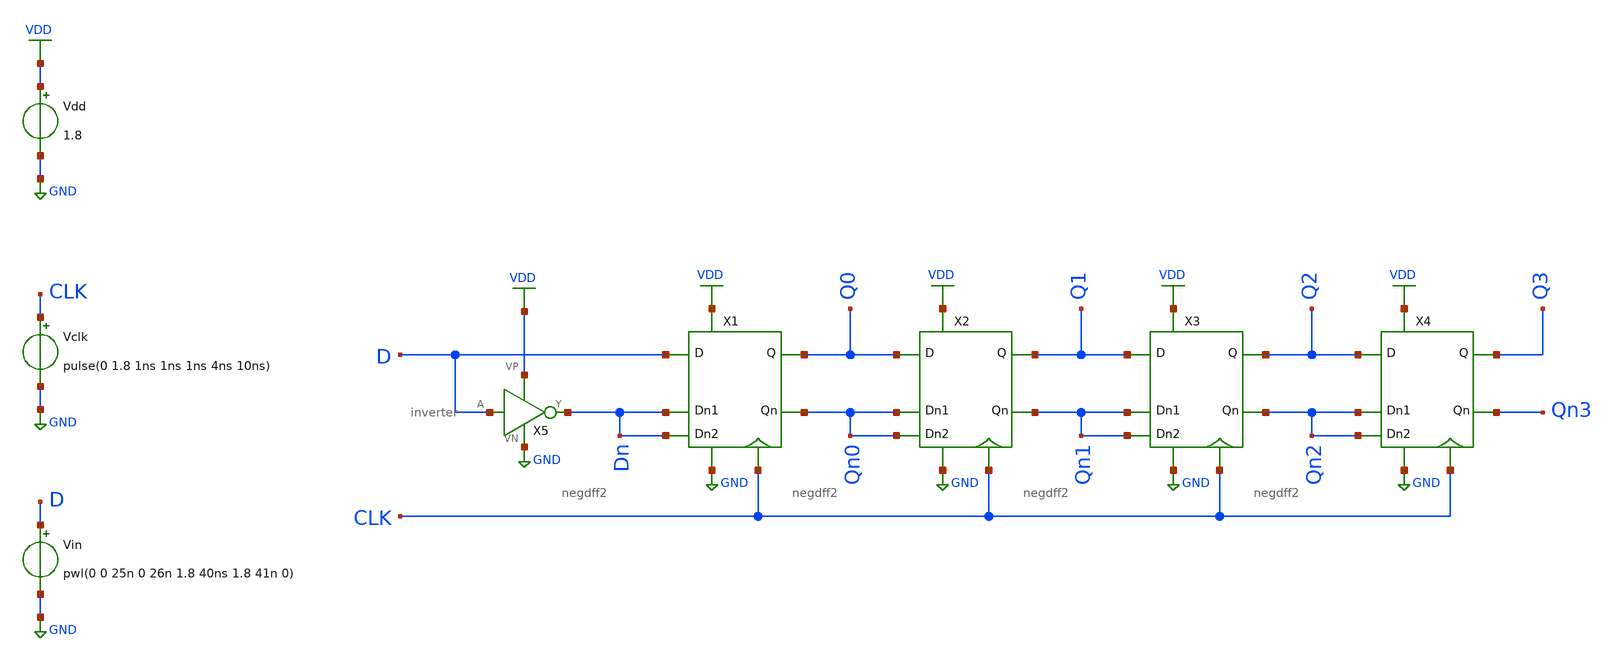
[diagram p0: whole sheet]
** sch_path: projects/negdff/xschem_ngspice/sreg_tran.sch
**.subckt sreg_tran
X1 VDD GND CLK D Dn Dn Q0 Qn0 negdff2
X2 VDD GND CLK Q0 Qn0 Qn0 Q1 Qn1 negdff2
X3 VDD GND CLK Q1 Qn1 Qn1 Q2 Qn2 negdff2
X4 VDD GND CLK Q2 Qn2 Qn2 Q3 Qn3 negdff2
X5 D Dn VDD GND inverter
Vin D GND pwl(0 0 25n 0 26n 1.8 40ns 1.8 41n 0)
Vdd VDD GND 1.8
Vclk CLK GND pulse(0 1.8 1ns 1ns 1ns 4ns 10ns)
**** begin user architecture code



.lib /foss/pdks/sky130A/libs.tech/ngspice/sky130.lib.spice tt

.ic v(Q0)=0 v(Q0)=0 v(Q1)=0 v(Q2)=0 v(Q3)=0

.tran 0.01n 100n

.save all



**** end user architecture code
**.ends

* expanding   symbol:  /foss/designs/my_design/projects/negdff/xschem_ngspice/negdff2.sym # of
*+ pins=8
** sym_path: projects/negdff/xschem_ngspice/negdff2.sym
** sch_path: projects/negdff/xschem_ngspice/negdff2.sch
.subckt negdff2 VP VN CLK D Dn1 Dn2 Q Qn
*.ipin D
*.ipin Dn1
*.ipin Dn2
*.opin Q
*.opin Qn
*.ipin CLK
*.iopin VP
*.iopin VN
XM1 net8 Dn2 VN VN sky130_fd_pr__nfet_01v8 L=0.15 W=1 nf=1 ad='int((nf+1)/2) * W/nf * 0.29' as='int((nf+2)/2) * W/nf * 0.29'
+ pd='2*int((nf+1)/2) * (W/nf + 0.29)' ps='2*int((nf+2)/2) * (W/nf + 0.29)' nrd='0.29 / W' nrs='0.29 / W'
+ sa=0 sb=0 sd=0 mult=1 m=1
XM2 net6 CLK net8 VN sky130_fd_pr__nfet_01v8 L=0.15 W=1 nf=1 ad='int((nf+1)/2) * W/nf * 0.29' as='int((nf+2)/2) * W/nf * 0.29'
+ pd='2*int((nf+1)/2) * (W/nf + 0.29)' ps='2*int((nf+2)/2) * (W/nf + 0.29)' nrd='0.29 / W' nrs='0.29 / W'
+ sa=0 sb=0 sd=0 mult=1 m=1
XM3 VN net1 net6 VN sky130_fd_pr__nfet_01v8 L=0.15 W=1 nf=1 ad='int((nf+1)/2) * W/nf * 0.29' as='int((nf+2)/2) * W/nf * 0.29'
+ pd='2*int((nf+1)/2) * (W/nf + 0.29)' ps='2*int((nf+2)/2) * (W/nf + 0.29)' nrd='0.29 / W' nrs='0.29 / W'
+ sa=0 sb=0 sd=0 mult=1 m=1
XM4 net7 D VN VN sky130_fd_pr__nfet_01v8 L=0.15 W=1 nf=1 ad='int((nf+1)/2) * W/nf * 0.29' as='int((nf+2)/2) * W/nf * 0.29'
+ pd='2*int((nf+1)/2) * (W/nf + 0.29)' ps='2*int((nf+2)/2) * (W/nf + 0.29)' nrd='0.29 / W' nrs='0.29 / W'
+ sa=0 sb=0 sd=0 mult=1 m=1
XM5 net7 CLK net1 VN sky130_fd_pr__nfet_01v8 L=0.15 W=1 nf=1 ad='int((nf+1)/2) * W/nf * 0.29' as='int((nf+2)/2) * W/nf * 0.29'
+ pd='2*int((nf+1)/2) * (W/nf + 0.29)' ps='2*int((nf+2)/2) * (W/nf + 0.29)' nrd='0.29 / W' nrs='0.29 / W'
+ sa=0 sb=0 sd=0 mult=1 m=1
XM6 net1 net6 VN VN sky130_fd_pr__nfet_01v8 L=0.15 W=1 nf=1 ad='int((nf+1)/2) * W/nf * 0.29' as='int((nf+2)/2) * W/nf * 0.29'
+ pd='2*int((nf+1)/2) * (W/nf + 0.29)' ps='2*int((nf+2)/2) * (W/nf + 0.29)' nrd='0.29 / W' nrs='0.29 / W'
+ sa=0 sb=0 sd=0 mult=1 m=1
XM7 net4 net6 VN VN sky130_fd_pr__nfet_01v8 L=0.15 W=1 nf=1 ad='int((nf+1)/2) * W/nf * 0.29' as='int((nf+2)/2) * W/nf * 0.29'
+ pd='2*int((nf+1)/2) * (W/nf + 0.29)' ps='2*int((nf+2)/2) * (W/nf + 0.29)' nrd='0.29 / W' nrs='0.29 / W'
+ sa=0 sb=0 sd=0 mult=1 m=1
XM8 net4 CLK VN VN sky130_fd_pr__nfet_01v8 L=0.15 W=1 nf=1 ad='int((nf+1)/2) * W/nf * 0.29' as='int((nf+2)/2) * W/nf * 0.29'
+ pd='2*int((nf+1)/2) * (W/nf + 0.29)' ps='2*int((nf+2)/2) * (W/nf + 0.29)' nrd='0.29 / W' nrs='0.29 / W'
+ sa=0 sb=0 sd=0 mult=1 m=1
XM9 Qn Q net4 VN sky130_fd_pr__nfet_01v8 L=0.15 W=1 nf=1 ad='int((nf+1)/2) * W/nf * 0.29' as='int((nf+2)/2) * W/nf * 0.29'
+ pd='2*int((nf+1)/2) * (W/nf + 0.29)' ps='2*int((nf+2)/2) * (W/nf + 0.29)' nrd='0.29 / W' nrs='0.29 / W'
+ sa=0 sb=0 sd=0 mult=1 m=1
XM10 net5 net1 VN VN sky130_fd_pr__nfet_01v8 L=0.15 W=1 nf=1 ad='int((nf+1)/2) * W/nf * 0.29' as='int((nf+2)/2) * W/nf * 0.29'
+ pd='2*int((nf+1)/2) * (W/nf + 0.29)' ps='2*int((nf+2)/2) * (W/nf + 0.29)' nrd='0.29 / W' nrs='0.29 / W'
+ sa=0 sb=0 sd=0 mult=1 m=1
XM11 net5 CLK VN VN sky130_fd_pr__nfet_01v8 L=0.15 W=1 nf=1 ad='int((nf+1)/2) * W/nf * 0.29' as='int((nf+2)/2) * W/nf * 0.29'
+ pd='2*int((nf+1)/2) * (W/nf + 0.29)' ps='2*int((nf+2)/2) * (W/nf + 0.29)' nrd='0.29 / W' nrs='0.29 / W'
+ sa=0 sb=0 sd=0 mult=1 m=1
XM12 Q Qn net5 VN sky130_fd_pr__nfet_01v8 L=0.15 W=1 nf=1 ad='int((nf+1)/2) * W/nf * 0.29' as='int((nf+2)/2) * W/nf * 0.29'
+ pd='2*int((nf+1)/2) * (W/nf + 0.29)' ps='2*int((nf+2)/2) * (W/nf + 0.29)' nrd='0.29 / W' nrs='0.29 / W'
+ sa=0 sb=0 sd=0 mult=1 m=1
XM13 net2 Dn1 VP VP sky130_fd_pr__pfet_01v8 L=0.15 W=1 nf=1 ad='int((nf+1)/2) * W/nf * 0.29' as='int((nf+2)/2) * W/nf * 0.29'
+ pd='2*int((nf+1)/2) * (W/nf + 0.29)' ps='2*int((nf+2)/2) * (W/nf + 0.29)' nrd='0.29 / W' nrs='0.29 / W'
+ sa=0 sb=0 sd=0 mult=1 m=1
XM14 net2 CLK VP VP sky130_fd_pr__pfet_01v8 L=0.15 W=1 nf=1 ad='int((nf+1)/2) * W/nf * 0.29' as='int((nf+2)/2) * W/nf * 0.29'
+ pd='2*int((nf+1)/2) * (W/nf + 0.29)' ps='2*int((nf+2)/2) * (W/nf + 0.29)' nrd='0.29 / W' nrs='0.29 / W'
+ sa=0 sb=0 sd=0 mult=1 m=1
XM15 net6 net1 net2 VP sky130_fd_pr__pfet_01v8 L=0.15 W=1 nf=1 ad='int((nf+1)/2) * W/nf * 0.29' as='int((nf+2)/2) * W/nf * 0.29'
+ pd='2*int((nf+1)/2) * (W/nf + 0.29)' ps='2*int((nf+2)/2) * (W/nf + 0.29)' nrd='0.29 / W' nrs='0.29 / W'
+ sa=0 sb=0 sd=0 mult=1 m=1
XM16 net1 net6 net3 VP sky130_fd_pr__pfet_01v8 L=0.15 W=1 nf=1 ad='int((nf+1)/2) * W/nf * 0.29' as='int((nf+2)/2) * W/nf * 0.29'
+ pd='2*int((nf+1)/2) * (W/nf + 0.29)' ps='2*int((nf+2)/2) * (W/nf + 0.29)' nrd='0.29 / W' nrs='0.29 / W'
+ sa=0 sb=0 sd=0 mult=1 m=1
XM17 net3 CLK VP VP sky130_fd_pr__pfet_01v8 L=0.15 W=1 nf=1 ad='int((nf+1)/2) * W/nf * 0.29' as='int((nf+2)/2) * W/nf * 0.29'
+ pd='2*int((nf+1)/2) * (W/nf + 0.29)' ps='2*int((nf+2)/2) * (W/nf + 0.29)' nrd='0.29 / W' nrs='0.29 / W'
+ sa=0 sb=0 sd=0 mult=1 m=1
XM18 net3 D VP VP sky130_fd_pr__pfet_01v8 L=0.15 W=1 nf=1 ad='int((nf+1)/2) * W/nf * 0.29' as='int((nf+2)/2) * W/nf * 0.29'
+ pd='2*int((nf+1)/2) * (W/nf + 0.29)' ps='2*int((nf+2)/2) * (W/nf + 0.29)' nrd='0.29 / W' nrs='0.29 / W'
+ sa=0 sb=0 sd=0 mult=1 m=1
XM19 net9 net1 VP VP sky130_fd_pr__pfet_01v8 L=0.15 W=1 nf=1 ad='int((nf+1)/2) * W/nf * 0.29' as='int((nf+2)/2) * W/nf * 0.29'
+ pd='2*int((nf+1)/2) * (W/nf + 0.29)' ps='2*int((nf+2)/2) * (W/nf + 0.29)' nrd='0.29 / W' nrs='0.29 / W'
+ sa=0 sb=0 sd=0 mult=1 m=1
XM20 net10 net6 VP VP sky130_fd_pr__pfet_01v8 L=0.15 W=1 nf=1 ad='int((nf+1)/2) * W/nf * 0.29' as='int((nf+2)/2) * W/nf * 0.29'
+ pd='2*int((nf+1)/2) * (W/nf + 0.29)' ps='2*int((nf+2)/2) * (W/nf + 0.29)' nrd='0.29 / W' nrs='0.29 / W'
+ sa=0 sb=0 sd=0 mult=1 m=1
XM21 Q CLK net9 VP sky130_fd_pr__pfet_01v8 L=0.15 W=1 nf=1 ad='int((nf+1)/2) * W/nf * 0.29' as='int((nf+2)/2) * W/nf * 0.29'
+ pd='2*int((nf+1)/2) * (W/nf + 0.29)' ps='2*int((nf+2)/2) * (W/nf + 0.29)' nrd='0.29 / W' nrs='0.29 / W'
+ sa=0 sb=0 sd=0 mult=1 m=1
XM22 Q Qn VP VP sky130_fd_pr__pfet_01v8 L=0.15 W=1 nf=1 ad='int((nf+1)/2) * W/nf * 0.29' as='int((nf+2)/2) * W/nf * 0.29'
+ pd='2*int((nf+1)/2) * (W/nf + 0.29)' ps='2*int((nf+2)/2) * (W/nf + 0.29)' nrd='0.29 / W' nrs='0.29 / W'
+ sa=0 sb=0 sd=0 mult=1 m=1
XM23 Qn Q VP VP sky130_fd_pr__pfet_01v8 L=0.15 W=1 nf=1 ad='int((nf+1)/2) * W/nf * 0.29' as='int((nf+2)/2) * W/nf * 0.29'
+ pd='2*int((nf+1)/2) * (W/nf + 0.29)' ps='2*int((nf+2)/2) * (W/nf + 0.29)' nrd='0.29 / W' nrs='0.29 / W'
+ sa=0 sb=0 sd=0 mult=1 m=1
XM24 Qn CLK net10 VP sky130_fd_pr__pfet_01v8 L=0.15 W=1 nf=1 ad='int((nf+1)/2) * W/nf * 0.29' as='int((nf+2)/2) * W/nf * 0.29'
+ pd='2*int((nf+1)/2) * (W/nf + 0.29)' ps='2*int((nf+2)/2) * (W/nf + 0.29)' nrd='0.29 / W' nrs='0.29 / W'
+ sa=0 sb=0 sd=0 mult=1 m=1
.ends


* expanding   symbol:
*+  /foss/designs/my_design/projects/inverter_tutorial/xschem_ngspice/inverter.sym # of pins=4
** sym_path: projects/inverter_tutorial/xschem_ngspice/inverter.sym
** sch_path: projects/inverter_tutorial/xschem_ngspice/inverter.sch
.subckt inverter A Y VP VN
*.ipin A
*.iopin VP
*.iopin VN
*.opin Y
XM1 Y A VN VN sky130_fd_pr__nfet_01v8 L=0.15 W=1 nf=1 ad='int((nf+1)/2) * W/nf * 0.29' as='int((nf+2)/2) * W/nf * 0.29'
+ pd='2*int((nf+1)/2) * (W/nf + 0.29)' ps='2*int((nf+2)/2) * (W/nf + 0.29)' nrd='0.29 / W' nrs='0.29 / W'
+ sa=0 sb=0 sd=0 mult=1 m=1
XM2 Y A VP VP sky130_fd_pr__pfet_01v8 L=0.15 W=1 nf=1 ad='int((nf+1)/2) * W/nf * 0.29' as='int((nf+2)/2) * W/nf * 0.29'
+ pd='2*int((nf+1)/2) * (W/nf + 0.29)' ps='2*int((nf+2)/2) * (W/nf + 0.29)' nrd='0.29 / W' nrs='0.29 / W'
+ sa=0 sb=0 sd=0 mult=1 m=1
.ends

.GLOBAL GND
.GLOBAL VDD
.end
